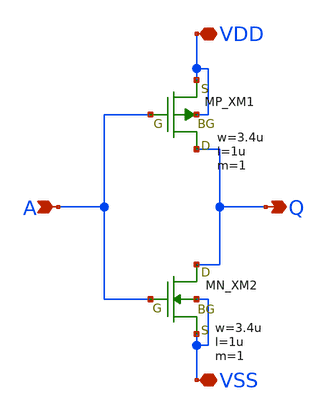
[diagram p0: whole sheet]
** sch_path: member_project/inverter/ichiken/soraoto06/inverter_soraoto06.sch
**.subckt inverter_soraoto06 A VDD Q VSS
*.ipin A
*.iopin VDD
*.opin Q
*.iopin VSS
XM1 Q A VDD VDD PMOS w=3.4u l=1u as=0 ad=0 ps=0 pd=0 nrd=0 nrs=0 m=1
XM2 Q A VSS VSS NMOS w=3.4u l=1u as=0 ad=0 ps=0 pd=0 nrd=0 nrs=0 m=1
**.ends
.end
